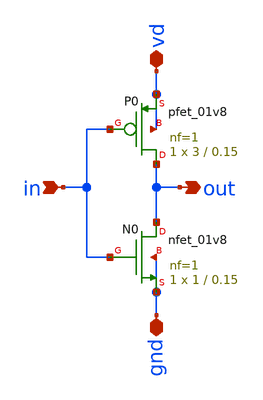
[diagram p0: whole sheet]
** sch_path: xschem/inverter-sky130.sch
**.subckt inverter-sky130 in vd gnd out
*.ipin in
*.iopin vd
*.iopin gnd
*.opin out
XN0 out in gnd gnd sky130_fd_pr__nfet_01v8 L=0.15 W=1 nf=1 ad='int((nf+1)/2) * W/nf * 0.29' as='int((nf+2)/2) * W/nf * 0.29'
+ pd='2*int((nf+1)/2) * (W/nf + 0.29)' ps='2*int((nf+2)/2) * (W/nf + 0.29)' nrd='0.29 / W' nrs='0.29 / W'
+ sa=0 sb=0 sd=0 mult=1 m=1
XP0 out in vd vd sky130_fd_pr__pfet_01v8 L=0.15 W=3 nf=1 ad='int((nf+1)/2) * W/nf * 0.29' as='int((nf+2)/2) * W/nf * 0.29'
+ pd='2*int((nf+1)/2) * (W/nf + 0.29)' ps='2*int((nf+2)/2) * (W/nf + 0.29)' nrd='0.29 / W' nrs='0.29 / W'
+ sa=0 sb=0 sd=0 mult=1 m=1
**.ends
.end
